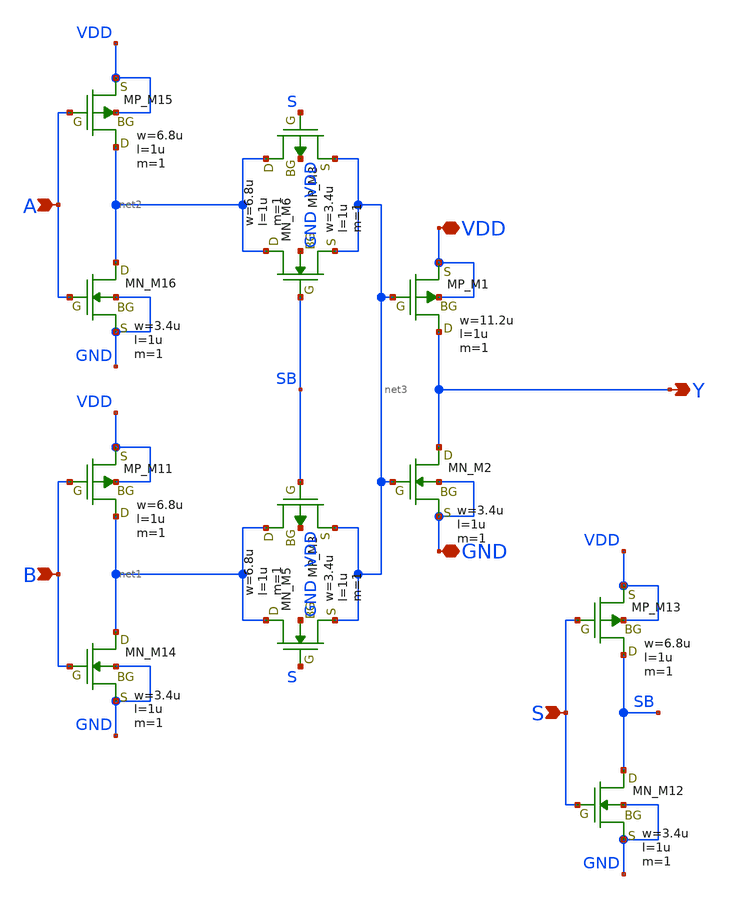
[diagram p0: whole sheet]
** sch_path: LEF/MUX2.sch
**.subckt MUX2 S Y VDD GND B A
*.ipin S
*.opin Y
*.iopin VDD
*.iopin GND
*.ipin B
*.ipin A
XM13 SB S VDD VDD PMOS w=6.8u l=1u as=0 ad=0 ps=0 pd=0 nrd=0 nrs=0 m=1
XM8 net2 S net3 VDD PMOS w=6.8u l=1u as=0 ad=0 ps=0 pd=0 nrd=0 nrs=0 m=1
XM12 SB S GND GND NMOS w=3.4u l=1u as=0 ad=0 ps=0 pd=0 nrd=0 nrs=0 m=1
XM6 net2 SB net3 GND NMOS w=3.4u l=1u as=0 ad=0 ps=0 pd=0 nrd=0 nrs=0 m=1
XM11 net1 B VDD VDD PMOS w=6.8u l=1u as=0 ad=0 ps=0 pd=0 nrd=0 nrs=0 m=1
XM14 net1 B GND GND NMOS w=3.4u l=1u as=0 ad=0 ps=0 pd=0 nrd=0 nrs=0 m=1
XM15 net2 A VDD VDD PMOS w=6.8u l=1u as=0 ad=0 ps=0 pd=0 nrd=0 nrs=0 m=1
XM16 net2 A GND GND NMOS w=3.4u l=1u as=0 ad=0 ps=0 pd=0 nrd=0 nrs=0 m=1
XM3 net1 SB net3 VDD PMOS w=6.8u l=1u as=0 ad=0 ps=0 pd=0 nrd=0 nrs=0 m=1
XM5 net1 S net3 GND NMOS w=3.4u l=1u as=0 ad=0 ps=0 pd=0 nrd=0 nrs=0 m=1
XM1 Y net3 VDD VDD PMOS w=11.2u l=1u as=0 ad=0 ps=0 pd=0 nrd=0 nrs=0 m=1
XM2 Y net3 GND GND NMOS w=3.4u l=1u as=0 ad=0 ps=0 pd=0 nrd=0 nrs=0 m=1
**.ends
.end
